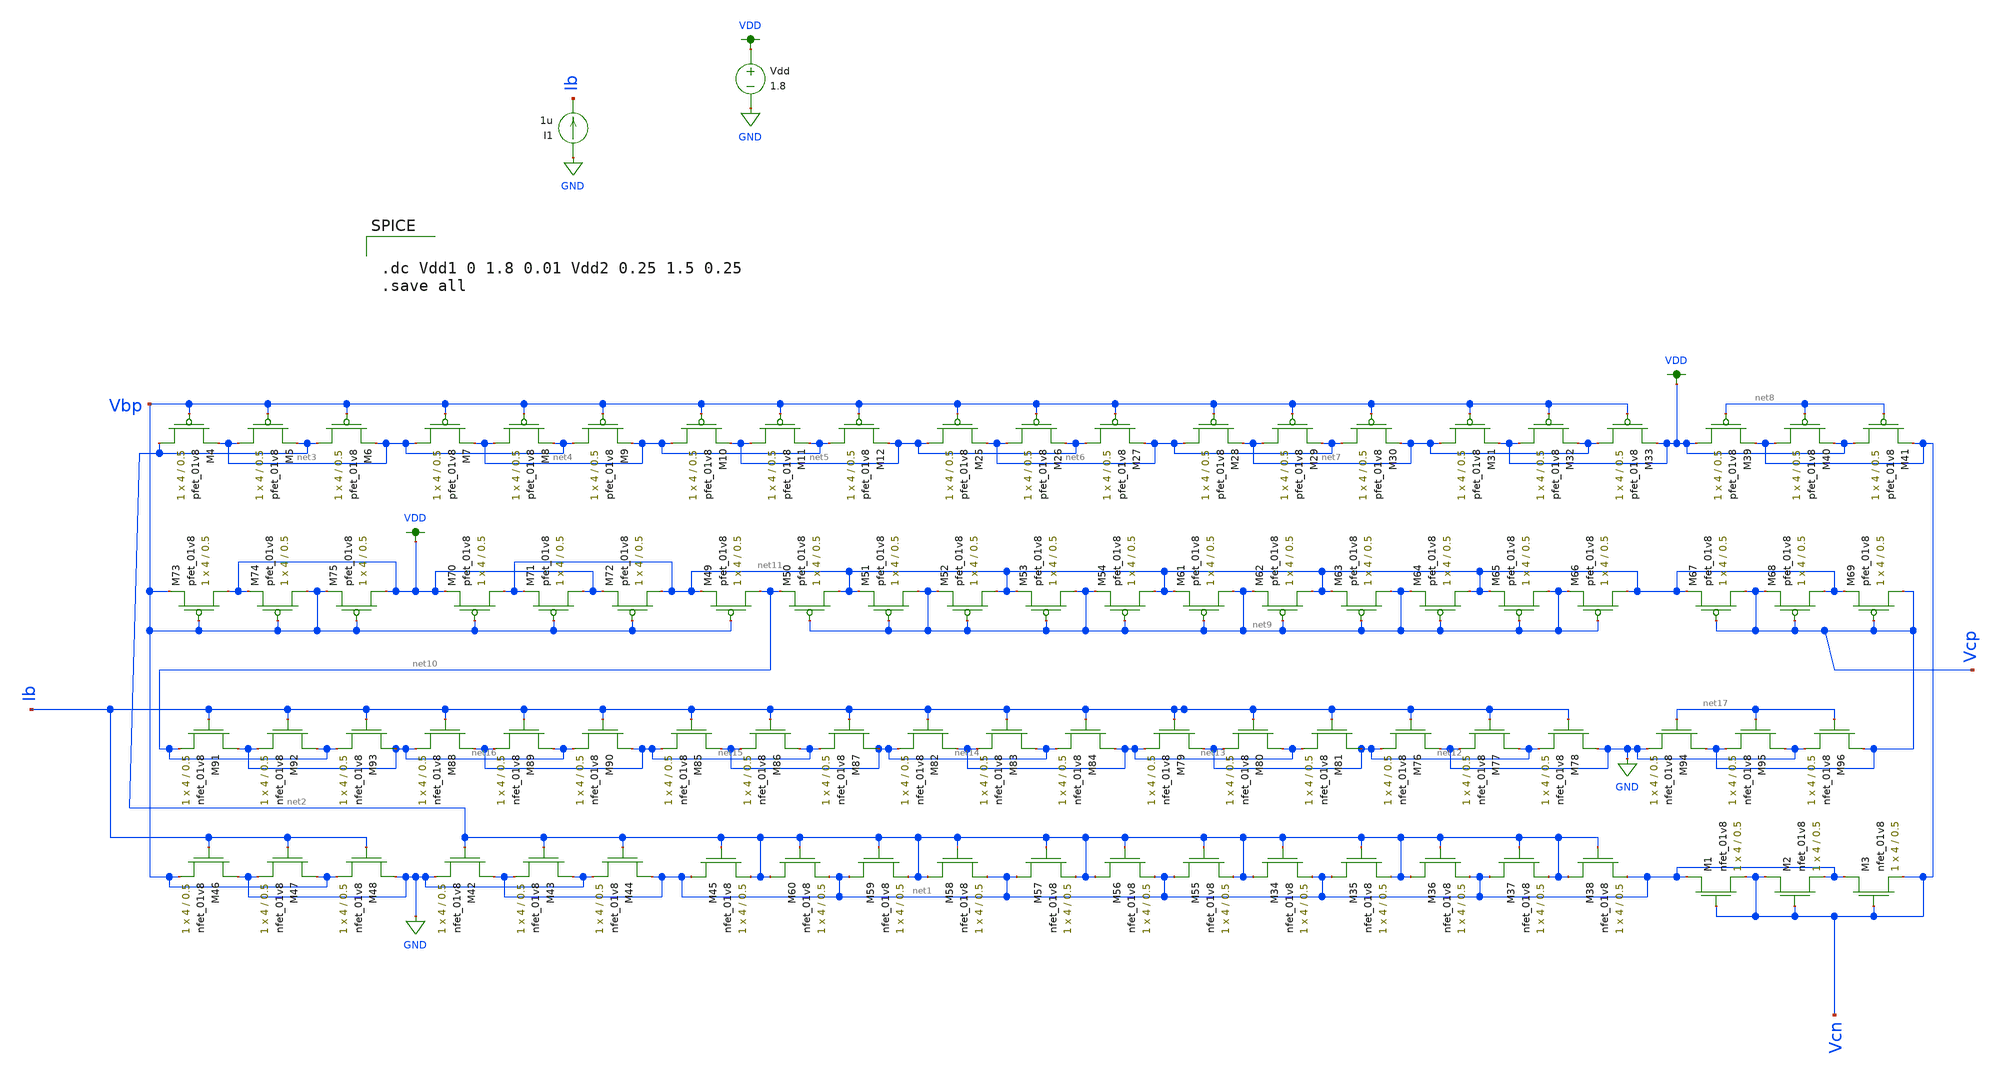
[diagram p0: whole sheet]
** sch_path: mp3/schematic/bias_lds.sch
**.subckt bias_lds
XM55 net1 net2 net2 GND sky130_fd_pr__nfet_01v8 L=0.5 W=4 nf=1 ad='int((nf+1)/2) * W/nf * 0.29' as='int((nf+2)/2) * W/nf * 0.29'
+ pd='2*int((nf+1)/2) * (W/nf + 0.29)' ps='2*int((nf+2)/2) * (W/nf + 0.29)' nrd='0.29 / W' nrs='0.29 / W'
+ sa=0 sb=0 sd=0 mult=1 m=1
XM56 net2 net2 net1 GND sky130_fd_pr__nfet_01v8 L=0.5 W=4 nf=1 ad='int((nf+1)/2) * W/nf * 0.29' as='int((nf+2)/2) * W/nf * 0.29'
+ pd='2*int((nf+1)/2) * (W/nf + 0.29)' ps='2*int((nf+2)/2) * (W/nf + 0.29)' nrd='0.29 / W' nrs='0.29 / W'
+ sa=0 sb=0 sd=0 mult=1 m=1
XM57 net1 net2 net2 GND sky130_fd_pr__nfet_01v8 L=0.5 W=4 nf=1 ad='int((nf+1)/2) * W/nf * 0.29' as='int((nf+2)/2) * W/nf * 0.29'
+ pd='2*int((nf+1)/2) * (W/nf + 0.29)' ps='2*int((nf+2)/2) * (W/nf + 0.29)' nrd='0.29 / W' nrs='0.29 / W'
+ sa=0 sb=0 sd=0 mult=1 m=1
XM58 net2 net2 net1 GND sky130_fd_pr__nfet_01v8 L=0.5 W=4 nf=1 ad='int((nf+1)/2) * W/nf * 0.29' as='int((nf+2)/2) * W/nf * 0.29'
+ pd='2*int((nf+1)/2) * (W/nf + 0.29)' ps='2*int((nf+2)/2) * (W/nf + 0.29)' nrd='0.29 / W' nrs='0.29 / W'
+ sa=0 sb=0 sd=0 mult=1 m=1
XM59 net1 net2 net2 GND sky130_fd_pr__nfet_01v8 L=0.5 W=4 nf=1 ad='int((nf+1)/2) * W/nf * 0.29' as='int((nf+2)/2) * W/nf * 0.29'
+ pd='2*int((nf+1)/2) * (W/nf + 0.29)' ps='2*int((nf+2)/2) * (W/nf + 0.29)' nrd='0.29 / W' nrs='0.29 / W'
+ sa=0 sb=0 sd=0 mult=1 m=1
XM60 net2 net2 net1 GND sky130_fd_pr__nfet_01v8 L=0.5 W=4 nf=1 ad='int((nf+1)/2) * W/nf * 0.29' as='int((nf+2)/2) * W/nf * 0.29'
+ pd='2*int((nf+1)/2) * (W/nf + 0.29)' ps='2*int((nf+2)/2) * (W/nf + 0.29)' nrd='0.29 / W' nrs='0.29 / W'
+ sa=0 sb=0 sd=0 mult=1 m=1
XM34 net2 net2 net1 GND sky130_fd_pr__nfet_01v8 L=0.5 W=4 nf=1 ad='int((nf+1)/2) * W/nf * 0.29' as='int((nf+2)/2) * W/nf * 0.29'
+ pd='2*int((nf+1)/2) * (W/nf + 0.29)' ps='2*int((nf+2)/2) * (W/nf + 0.29)' nrd='0.29 / W' nrs='0.29 / W'
+ sa=0 sb=0 sd=0 mult=1 m=1
XM35 net1 net2 net2 GND sky130_fd_pr__nfet_01v8 L=0.5 W=4 nf=1 ad='int((nf+1)/2) * W/nf * 0.29' as='int((nf+2)/2) * W/nf * 0.29'
+ pd='2*int((nf+1)/2) * (W/nf + 0.29)' ps='2*int((nf+2)/2) * (W/nf + 0.29)' nrd='0.29 / W' nrs='0.29 / W'
+ sa=0 sb=0 sd=0 mult=1 m=1
XM36 net2 net2 net1 GND sky130_fd_pr__nfet_01v8 L=0.5 W=4 nf=1 ad='int((nf+1)/2) * W/nf * 0.29' as='int((nf+2)/2) * W/nf * 0.29'
+ pd='2*int((nf+1)/2) * (W/nf + 0.29)' ps='2*int((nf+2)/2) * (W/nf + 0.29)' nrd='0.29 / W' nrs='0.29 / W'
+ sa=0 sb=0 sd=0 mult=1 m=1
XM37 net1 net2 net2 GND sky130_fd_pr__nfet_01v8 L=0.5 W=4 nf=1 ad='int((nf+1)/2) * W/nf * 0.29' as='int((nf+2)/2) * W/nf * 0.29'
+ pd='2*int((nf+1)/2) * (W/nf + 0.29)' ps='2*int((nf+2)/2) * (W/nf + 0.29)' nrd='0.29 / W' nrs='0.29 / W'
+ sa=0 sb=0 sd=0 mult=1 m=1
XM38 net2 net2 net1 GND sky130_fd_pr__nfet_01v8 L=0.5 W=4 nf=1 ad='int((nf+1)/2) * W/nf * 0.29' as='int((nf+2)/2) * W/nf * 0.29'
+ pd='2*int((nf+1)/2) * (W/nf + 0.29)' ps='2*int((nf+2)/2) * (W/nf + 0.29)' nrd='0.29 / W' nrs='0.29 / W'
+ sa=0 sb=0 sd=0 mult=1 m=1
XM45 net1 net2 net2 GND sky130_fd_pr__nfet_01v8 L=0.5 W=4 nf=1 ad='int((nf+1)/2) * W/nf * 0.29' as='int((nf+2)/2) * W/nf * 0.29'
+ pd='2*int((nf+1)/2) * (W/nf + 0.29)' ps='2*int((nf+2)/2) * (W/nf + 0.29)' nrd='0.29 / W' nrs='0.29 / W'
+ sa=0 sb=0 sd=0 mult=1 m=1
XM1 net1 Vcn Vcn GND sky130_fd_pr__nfet_01v8 L=0.5 W=4 nf=1 ad='int((nf+1)/2) * W/nf * 0.29' as='int((nf+2)/2) * W/nf * 0.29'
+ pd='2*int((nf+1)/2) * (W/nf + 0.29)' ps='2*int((nf+2)/2) * (W/nf + 0.29)' nrd='0.29 / W' nrs='0.29 / W'
+ sa=0 sb=0 sd=0 mult=1 m=1
XM2 Vcn Vcn net1 GND sky130_fd_pr__nfet_01v8 L=0.5 W=4 nf=1 ad='int((nf+1)/2) * W/nf * 0.29' as='int((nf+2)/2) * W/nf * 0.29'
+ pd='2*int((nf+1)/2) * (W/nf + 0.29)' ps='2*int((nf+2)/2) * (W/nf + 0.29)' nrd='0.29 / W' nrs='0.29 / W'
+ sa=0 sb=0 sd=0 mult=1 m=1
XM3 net1 Vcn Vcn GND sky130_fd_pr__nfet_01v8 L=0.5 W=4 nf=1 ad='int((nf+1)/2) * W/nf * 0.29' as='int((nf+2)/2) * W/nf * 0.29'
+ pd='2*int((nf+1)/2) * (W/nf + 0.29)' ps='2*int((nf+2)/2) * (W/nf + 0.29)' nrd='0.29 / W' nrs='0.29 / W'
+ sa=0 sb=0 sd=0 mult=1 m=1
XM4 net2 Vbp net3 VDD sky130_fd_pr__pfet_01v8 L=0.5 W=4 nf=1 ad='int((nf+1)/2) * W/nf * 0.29' as='int((nf+2)/2) * W/nf * 0.29'
+ pd='2*int((nf+1)/2) * (W/nf + 0.29)' ps='2*int((nf+2)/2) * (W/nf + 0.29)' nrd='0.29 / W' nrs='0.29 / W'
+ sa=0 sb=0 sd=0 mult=1 m=1
XM5 net3 Vbp net2 VDD sky130_fd_pr__pfet_01v8 L=0.5 W=4 nf=1 ad='int((nf+1)/2) * W/nf * 0.29' as='int((nf+2)/2) * W/nf * 0.29'
+ pd='2*int((nf+1)/2) * (W/nf + 0.29)' ps='2*int((nf+2)/2) * (W/nf + 0.29)' nrd='0.29 / W' nrs='0.29 / W'
+ sa=0 sb=0 sd=0 mult=1 m=1
XM6 net2 Vbp net3 VDD sky130_fd_pr__pfet_01v8 L=0.5 W=4 nf=1 ad='int((nf+1)/2) * W/nf * 0.29' as='int((nf+2)/2) * W/nf * 0.29'
+ pd='2*int((nf+1)/2) * (W/nf + 0.29)' ps='2*int((nf+2)/2) * (W/nf + 0.29)' nrd='0.29 / W' nrs='0.29 / W'
+ sa=0 sb=0 sd=0 mult=1 m=1
XM7 net3 Vbp net4 VDD sky130_fd_pr__pfet_01v8 L=0.5 W=4 nf=1 ad='int((nf+1)/2) * W/nf * 0.29' as='int((nf+2)/2) * W/nf * 0.29'
+ pd='2*int((nf+1)/2) * (W/nf + 0.29)' ps='2*int((nf+2)/2) * (W/nf + 0.29)' nrd='0.29 / W' nrs='0.29 / W'
+ sa=0 sb=0 sd=0 mult=1 m=1
XM8 net4 Vbp net3 VDD sky130_fd_pr__pfet_01v8 L=0.5 W=4 nf=1 ad='int((nf+1)/2) * W/nf * 0.29' as='int((nf+2)/2) * W/nf * 0.29'
+ pd='2*int((nf+1)/2) * (W/nf + 0.29)' ps='2*int((nf+2)/2) * (W/nf + 0.29)' nrd='0.29 / W' nrs='0.29 / W'
+ sa=0 sb=0 sd=0 mult=1 m=1
XM9 net3 Vbp net4 VDD sky130_fd_pr__pfet_01v8 L=0.5 W=4 nf=1 ad='int((nf+1)/2) * W/nf * 0.29' as='int((nf+2)/2) * W/nf * 0.29'
+ pd='2*int((nf+1)/2) * (W/nf + 0.29)' ps='2*int((nf+2)/2) * (W/nf + 0.29)' nrd='0.29 / W' nrs='0.29 / W'
+ sa=0 sb=0 sd=0 mult=1 m=1
XM10 net4 Vbp net5 VDD sky130_fd_pr__pfet_01v8 L=0.5 W=4 nf=1 ad='int((nf+1)/2) * W/nf * 0.29' as='int((nf+2)/2) * W/nf * 0.29'
+ pd='2*int((nf+1)/2) * (W/nf + 0.29)' ps='2*int((nf+2)/2) * (W/nf + 0.29)' nrd='0.29 / W' nrs='0.29 / W'
+ sa=0 sb=0 sd=0 mult=1 m=1
XM11 net5 Vbp net4 VDD sky130_fd_pr__pfet_01v8 L=0.5 W=4 nf=1 ad='int((nf+1)/2) * W/nf * 0.29' as='int((nf+2)/2) * W/nf * 0.29'
+ pd='2*int((nf+1)/2) * (W/nf + 0.29)' ps='2*int((nf+2)/2) * (W/nf + 0.29)' nrd='0.29 / W' nrs='0.29 / W'
+ sa=0 sb=0 sd=0 mult=1 m=1
XM12 net4 Vbp net5 VDD sky130_fd_pr__pfet_01v8 L=0.5 W=4 nf=1 ad='int((nf+1)/2) * W/nf * 0.29' as='int((nf+2)/2) * W/nf * 0.29'
+ pd='2*int((nf+1)/2) * (W/nf + 0.29)' ps='2*int((nf+2)/2) * (W/nf + 0.29)' nrd='0.29 / W' nrs='0.29 / W'
+ sa=0 sb=0 sd=0 mult=1 m=1
XM25 net5 Vbp net6 VDD sky130_fd_pr__pfet_01v8 L=0.5 W=4 nf=1 ad='int((nf+1)/2) * W/nf * 0.29' as='int((nf+2)/2) * W/nf * 0.29'
+ pd='2*int((nf+1)/2) * (W/nf + 0.29)' ps='2*int((nf+2)/2) * (W/nf + 0.29)' nrd='0.29 / W' nrs='0.29 / W'
+ sa=0 sb=0 sd=0 mult=1 m=1
XM26 net6 Vbp net5 VDD sky130_fd_pr__pfet_01v8 L=0.5 W=4 nf=1 ad='int((nf+1)/2) * W/nf * 0.29' as='int((nf+2)/2) * W/nf * 0.29'
+ pd='2*int((nf+1)/2) * (W/nf + 0.29)' ps='2*int((nf+2)/2) * (W/nf + 0.29)' nrd='0.29 / W' nrs='0.29 / W'
+ sa=0 sb=0 sd=0 mult=1 m=1
XM27 net5 Vbp net6 VDD sky130_fd_pr__pfet_01v8 L=0.5 W=4 nf=1 ad='int((nf+1)/2) * W/nf * 0.29' as='int((nf+2)/2) * W/nf * 0.29'
+ pd='2*int((nf+1)/2) * (W/nf + 0.29)' ps='2*int((nf+2)/2) * (W/nf + 0.29)' nrd='0.29 / W' nrs='0.29 / W'
+ sa=0 sb=0 sd=0 mult=1 m=1
XM28 net6 Vbp net7 VDD sky130_fd_pr__pfet_01v8 L=0.5 W=4 nf=1 ad='int((nf+1)/2) * W/nf * 0.29' as='int((nf+2)/2) * W/nf * 0.29'
+ pd='2*int((nf+1)/2) * (W/nf + 0.29)' ps='2*int((nf+2)/2) * (W/nf + 0.29)' nrd='0.29 / W' nrs='0.29 / W'
+ sa=0 sb=0 sd=0 mult=1 m=1
XM29 net7 Vbp net6 VDD sky130_fd_pr__pfet_01v8 L=0.5 W=4 nf=1 ad='int((nf+1)/2) * W/nf * 0.29' as='int((nf+2)/2) * W/nf * 0.29'
+ pd='2*int((nf+1)/2) * (W/nf + 0.29)' ps='2*int((nf+2)/2) * (W/nf + 0.29)' nrd='0.29 / W' nrs='0.29 / W'
+ sa=0 sb=0 sd=0 mult=1 m=1
XM30 net6 Vbp net7 VDD sky130_fd_pr__pfet_01v8 L=0.5 W=4 nf=1 ad='int((nf+1)/2) * W/nf * 0.29' as='int((nf+2)/2) * W/nf * 0.29'
+ pd='2*int((nf+1)/2) * (W/nf + 0.29)' ps='2*int((nf+2)/2) * (W/nf + 0.29)' nrd='0.29 / W' nrs='0.29 / W'
+ sa=0 sb=0 sd=0 mult=1 m=1
XM31 net7 Vbp VDD VDD sky130_fd_pr__pfet_01v8 L=0.5 W=4 nf=1 ad='int((nf+1)/2) * W/nf * 0.29' as='int((nf+2)/2) * W/nf * 0.29'
+ pd='2*int((nf+1)/2) * (W/nf + 0.29)' ps='2*int((nf+2)/2) * (W/nf + 0.29)' nrd='0.29 / W' nrs='0.29 / W'
+ sa=0 sb=0 sd=0 mult=1 m=1
XM32 VDD Vbp net7 VDD sky130_fd_pr__pfet_01v8 L=0.5 W=4 nf=1 ad='int((nf+1)/2) * W/nf * 0.29' as='int((nf+2)/2) * W/nf * 0.29'
+ pd='2*int((nf+1)/2) * (W/nf + 0.29)' ps='2*int((nf+2)/2) * (W/nf + 0.29)' nrd='0.29 / W' nrs='0.29 / W'
+ sa=0 sb=0 sd=0 mult=1 m=1
XM33 net7 Vbp VDD VDD sky130_fd_pr__pfet_01v8 L=0.5 W=4 nf=1 ad='int((nf+1)/2) * W/nf * 0.29' as='int((nf+2)/2) * W/nf * 0.29'
+ pd='2*int((nf+1)/2) * (W/nf + 0.29)' ps='2*int((nf+2)/2) * (W/nf + 0.29)' nrd='0.29 / W' nrs='0.29 / W'
+ sa=0 sb=0 sd=0 mult=1 m=1
XM39 VDD net8 Vcn VDD sky130_fd_pr__pfet_01v8 L=0.5 W=4 nf=1 ad='int((nf+1)/2) * W/nf * 0.29' as='int((nf+2)/2) * W/nf * 0.29'
+ pd='2*int((nf+1)/2) * (W/nf + 0.29)' ps='2*int((nf+2)/2) * (W/nf + 0.29)' nrd='0.29 / W' nrs='0.29 / W'
+ sa=0 sb=0 sd=0 mult=1 m=1
XM40 Vcn net8 VDD VDD sky130_fd_pr__pfet_01v8 L=0.5 W=4 nf=1 ad='int((nf+1)/2) * W/nf * 0.29' as='int((nf+2)/2) * W/nf * 0.29'
+ pd='2*int((nf+1)/2) * (W/nf + 0.29)' ps='2*int((nf+2)/2) * (W/nf + 0.29)' nrd='0.29 / W' nrs='0.29 / W'
+ sa=0 sb=0 sd=0 mult=1 m=1
XM41 VDD net8 Vcn VDD sky130_fd_pr__pfet_01v8 L=0.5 W=4 nf=1 ad='int((nf+1)/2) * W/nf * 0.29' as='int((nf+2)/2) * W/nf * 0.29'
+ pd='2*int((nf+1)/2) * (W/nf + 0.29)' ps='2*int((nf+2)/2) * (W/nf + 0.29)' nrd='0.29 / W' nrs='0.29 / W'
+ sa=0 sb=0 sd=0 mult=1 m=1
XM42 net1 net2 GND GND sky130_fd_pr__nfet_01v8 L=0.5 W=4 nf=1 ad='int((nf+1)/2) * W/nf * 0.29' as='int((nf+2)/2) * W/nf * 0.29'
+ pd='2*int((nf+1)/2) * (W/nf + 0.29)' ps='2*int((nf+2)/2) * (W/nf + 0.29)' nrd='0.29 / W' nrs='0.29 / W'
+ sa=0 sb=0 sd=0 mult=1 m=1
XM43 GND net2 net1 GND sky130_fd_pr__nfet_01v8 L=0.5 W=4 nf=1 ad='int((nf+1)/2) * W/nf * 0.29' as='int((nf+2)/2) * W/nf * 0.29'
+ pd='2*int((nf+1)/2) * (W/nf + 0.29)' ps='2*int((nf+2)/2) * (W/nf + 0.29)' nrd='0.29 / W' nrs='0.29 / W'
+ sa=0 sb=0 sd=0 mult=1 m=1
XM44 net1 net2 GND GND sky130_fd_pr__nfet_01v8 L=0.5 W=4 nf=1 ad='int((nf+1)/2) * W/nf * 0.29' as='int((nf+2)/2) * W/nf * 0.29'
+ pd='2*int((nf+1)/2) * (W/nf + 0.29)' ps='2*int((nf+2)/2) * (W/nf + 0.29)' nrd='0.29 / W' nrs='0.29 / W'
+ sa=0 sb=0 sd=0 mult=1 m=1
XM46 GND Ib Vbp GND sky130_fd_pr__nfet_01v8 L=0.5 W=4 nf=1 ad='int((nf+1)/2) * W/nf * 0.29' as='int((nf+2)/2) * W/nf * 0.29'
+ pd='2*int((nf+1)/2) * (W/nf + 0.29)' ps='2*int((nf+2)/2) * (W/nf + 0.29)' nrd='0.29 / W' nrs='0.29 / W'
+ sa=0 sb=0 sd=0 mult=1 m=1
XM47 Vbp Ib GND GND sky130_fd_pr__nfet_01v8 L=0.5 W=4 nf=1 ad='int((nf+1)/2) * W/nf * 0.29' as='int((nf+2)/2) * W/nf * 0.29'
+ pd='2*int((nf+1)/2) * (W/nf + 0.29)' ps='2*int((nf+2)/2) * (W/nf + 0.29)' nrd='0.29 / W' nrs='0.29 / W'
+ sa=0 sb=0 sd=0 mult=1 m=1
XM48 GND Ib Vbp GND sky130_fd_pr__nfet_01v8 L=0.5 W=4 nf=1 ad='int((nf+1)/2) * W/nf * 0.29' as='int((nf+2)/2) * W/nf * 0.29'
+ pd='2*int((nf+1)/2) * (W/nf + 0.29)' ps='2*int((nf+2)/2) * (W/nf + 0.29)' nrd='0.29 / W' nrs='0.29 / W'
+ sa=0 sb=0 sd=0 mult=1 m=1
XM49 net10 Vbp net11 VDD sky130_fd_pr__pfet_01v8 L=0.5 W=4 nf=1 ad='int((nf+1)/2) * W/nf * 0.29' as='int((nf+2)/2) * W/nf * 0.29'
+ pd='2*int((nf+1)/2) * (W/nf + 0.29)' ps='2*int((nf+2)/2) * (W/nf + 0.29)' nrd='0.29 / W' nrs='0.29 / W'
+ sa=0 sb=0 sd=0 mult=1 m=1
XM50 net11 net9 net10 VDD sky130_fd_pr__pfet_01v8 L=0.5 W=4 nf=1 ad='int((nf+1)/2) * W/nf * 0.29' as='int((nf+2)/2) * W/nf * 0.29'
+ pd='2*int((nf+1)/2) * (W/nf + 0.29)' ps='2*int((nf+2)/2) * (W/nf + 0.29)' nrd='0.29 / W' nrs='0.29 / W'
+ sa=0 sb=0 sd=0 mult=1 m=1
XM51 net9 net9 net11 VDD sky130_fd_pr__pfet_01v8 L=0.5 W=4 nf=1 ad='int((nf+1)/2) * W/nf * 0.29' as='int((nf+2)/2) * W/nf * 0.29'
+ pd='2*int((nf+1)/2) * (W/nf + 0.29)' ps='2*int((nf+2)/2) * (W/nf + 0.29)' nrd='0.29 / W' nrs='0.29 / W'
+ sa=0 sb=0 sd=0 mult=1 m=1
XM52 net11 net9 net9 VDD sky130_fd_pr__pfet_01v8 L=0.5 W=4 nf=1 ad='int((nf+1)/2) * W/nf * 0.29' as='int((nf+2)/2) * W/nf * 0.29'
+ pd='2*int((nf+1)/2) * (W/nf + 0.29)' ps='2*int((nf+2)/2) * (W/nf + 0.29)' nrd='0.29 / W' nrs='0.29 / W'
+ sa=0 sb=0 sd=0 mult=1 m=1
XM53 net9 net9 net11 VDD sky130_fd_pr__pfet_01v8 L=0.5 W=4 nf=1 ad='int((nf+1)/2) * W/nf * 0.29' as='int((nf+2)/2) * W/nf * 0.29'
+ pd='2*int((nf+1)/2) * (W/nf + 0.29)' ps='2*int((nf+2)/2) * (W/nf + 0.29)' nrd='0.29 / W' nrs='0.29 / W'
+ sa=0 sb=0 sd=0 mult=1 m=1
XM54 net11 net9 net9 VDD sky130_fd_pr__pfet_01v8 L=0.5 W=4 nf=1 ad='int((nf+1)/2) * W/nf * 0.29' as='int((nf+2)/2) * W/nf * 0.29'
+ pd='2*int((nf+1)/2) * (W/nf + 0.29)' ps='2*int((nf+2)/2) * (W/nf + 0.29)' nrd='0.29 / W' nrs='0.29 / W'
+ sa=0 sb=0 sd=0 mult=1 m=1
XM61 net9 net9 net11 VDD sky130_fd_pr__pfet_01v8 L=0.5 W=4 nf=1 ad='int((nf+1)/2) * W/nf * 0.29' as='int((nf+2)/2) * W/nf * 0.29'
+ pd='2*int((nf+1)/2) * (W/nf + 0.29)' ps='2*int((nf+2)/2) * (W/nf + 0.29)' nrd='0.29 / W' nrs='0.29 / W'
+ sa=0 sb=0 sd=0 mult=1 m=1
XM62 net11 net9 net9 VDD sky130_fd_pr__pfet_01v8 L=0.5 W=4 nf=1 ad='int((nf+1)/2) * W/nf * 0.29' as='int((nf+2)/2) * W/nf * 0.29'
+ pd='2*int((nf+1)/2) * (W/nf + 0.29)' ps='2*int((nf+2)/2) * (W/nf + 0.29)' nrd='0.29 / W' nrs='0.29 / W'
+ sa=0 sb=0 sd=0 mult=1 m=1
XM63 net9 net9 net11 VDD sky130_fd_pr__pfet_01v8 L=0.5 W=4 nf=1 ad='int((nf+1)/2) * W/nf * 0.29' as='int((nf+2)/2) * W/nf * 0.29'
+ pd='2*int((nf+1)/2) * (W/nf + 0.29)' ps='2*int((nf+2)/2) * (W/nf + 0.29)' nrd='0.29 / W' nrs='0.29 / W'
+ sa=0 sb=0 sd=0 mult=1 m=1
XM64 net11 net9 net9 VDD sky130_fd_pr__pfet_01v8 L=0.5 W=4 nf=1 ad='int((nf+1)/2) * W/nf * 0.29' as='int((nf+2)/2) * W/nf * 0.29'
+ pd='2*int((nf+1)/2) * (W/nf + 0.29)' ps='2*int((nf+2)/2) * (W/nf + 0.29)' nrd='0.29 / W' nrs='0.29 / W'
+ sa=0 sb=0 sd=0 mult=1 m=1
XM65 net9 net9 net11 VDD sky130_fd_pr__pfet_01v8 L=0.5 W=4 nf=1 ad='int((nf+1)/2) * W/nf * 0.29' as='int((nf+2)/2) * W/nf * 0.29'
+ pd='2*int((nf+1)/2) * (W/nf + 0.29)' ps='2*int((nf+2)/2) * (W/nf + 0.29)' nrd='0.29 / W' nrs='0.29 / W'
+ sa=0 sb=0 sd=0 mult=1 m=1
XM66 net11 net9 net9 VDD sky130_fd_pr__pfet_01v8 L=0.5 W=4 nf=1 ad='int((nf+1)/2) * W/nf * 0.29' as='int((nf+2)/2) * W/nf * 0.29'
+ pd='2*int((nf+1)/2) * (W/nf + 0.29)' ps='2*int((nf+2)/2) * (W/nf + 0.29)' nrd='0.29 / W' nrs='0.29 / W'
+ sa=0 sb=0 sd=0 mult=1 m=1
XM67 Vcp Vcp net11 VDD sky130_fd_pr__pfet_01v8 L=0.5 W=4 nf=1 ad='int((nf+1)/2) * W/nf * 0.29' as='int((nf+2)/2) * W/nf * 0.29'
+ pd='2*int((nf+1)/2) * (W/nf + 0.29)' ps='2*int((nf+2)/2) * (W/nf + 0.29)' nrd='0.29 / W' nrs='0.29 / W'
+ sa=0 sb=0 sd=0 mult=1 m=1
XM68 net11 Vcp Vcp VDD sky130_fd_pr__pfet_01v8 L=0.5 W=4 nf=1 ad='int((nf+1)/2) * W/nf * 0.29' as='int((nf+2)/2) * W/nf * 0.29'
+ pd='2*int((nf+1)/2) * (W/nf + 0.29)' ps='2*int((nf+2)/2) * (W/nf + 0.29)' nrd='0.29 / W' nrs='0.29 / W'
+ sa=0 sb=0 sd=0 mult=1 m=1
XM69 Vcp Vcp net11 VDD sky130_fd_pr__pfet_01v8 L=0.5 W=4 nf=1 ad='int((nf+1)/2) * W/nf * 0.29' as='int((nf+2)/2) * W/nf * 0.29'
+ pd='2*int((nf+1)/2) * (W/nf + 0.29)' ps='2*int((nf+2)/2) * (W/nf + 0.29)' nrd='0.29 / W' nrs='0.29 / W'
+ sa=0 sb=0 sd=0 mult=1 m=1
XM70 net11 Vbp VDD VDD sky130_fd_pr__pfet_01v8 L=0.5 W=4 nf=1 ad='int((nf+1)/2) * W/nf * 0.29' as='int((nf+2)/2) * W/nf * 0.29'
+ pd='2*int((nf+1)/2) * (W/nf + 0.29)' ps='2*int((nf+2)/2) * (W/nf + 0.29)' nrd='0.29 / W' nrs='0.29 / W'
+ sa=0 sb=0 sd=0 mult=1 m=1
XM71 VDD Vbp net11 VDD sky130_fd_pr__pfet_01v8 L=0.5 W=4 nf=1 ad='int((nf+1)/2) * W/nf * 0.29' as='int((nf+2)/2) * W/nf * 0.29'
+ pd='2*int((nf+1)/2) * (W/nf + 0.29)' ps='2*int((nf+2)/2) * (W/nf + 0.29)' nrd='0.29 / W' nrs='0.29 / W'
+ sa=0 sb=0 sd=0 mult=1 m=1
XM72 net11 Vbp VDD VDD sky130_fd_pr__pfet_01v8 L=0.5 W=4 nf=1 ad='int((nf+1)/2) * W/nf * 0.29' as='int((nf+2)/2) * W/nf * 0.29'
+ pd='2*int((nf+1)/2) * (W/nf + 0.29)' ps='2*int((nf+2)/2) * (W/nf + 0.29)' nrd='0.29 / W' nrs='0.29 / W'
+ sa=0 sb=0 sd=0 mult=1 m=1
XM73 VDD Vbp Vbp VDD sky130_fd_pr__pfet_01v8 L=0.5 W=4 nf=1 ad='int((nf+1)/2) * W/nf * 0.29' as='int((nf+2)/2) * W/nf * 0.29'
+ pd='2*int((nf+1)/2) * (W/nf + 0.29)' ps='2*int((nf+2)/2) * (W/nf + 0.29)' nrd='0.29 / W' nrs='0.29 / W'
+ sa=0 sb=0 sd=0 mult=1 m=1
XM74 Vbp Vbp VDD VDD sky130_fd_pr__pfet_01v8 L=0.5 W=4 nf=1 ad='int((nf+1)/2) * W/nf * 0.29' as='int((nf+2)/2) * W/nf * 0.29'
+ pd='2*int((nf+1)/2) * (W/nf + 0.29)' ps='2*int((nf+2)/2) * (W/nf + 0.29)' nrd='0.29 / W' nrs='0.29 / W'
+ sa=0 sb=0 sd=0 mult=1 m=1
XM75 VDD Vbp Vbp VDD sky130_fd_pr__pfet_01v8 L=0.5 W=4 nf=1 ad='int((nf+1)/2) * W/nf * 0.29' as='int((nf+2)/2) * W/nf * 0.29'
+ pd='2*int((nf+1)/2) * (W/nf + 0.29)' ps='2*int((nf+2)/2) * (W/nf + 0.29)' nrd='0.29 / W' nrs='0.29 / W'
+ sa=0 sb=0 sd=0 mult=1 m=1
XM76 GND Ib net12 GND sky130_fd_pr__nfet_01v8 L=0.5 W=4 nf=1 ad='int((nf+1)/2) * W/nf * 0.29' as='int((nf+2)/2) * W/nf * 0.29'
+ pd='2*int((nf+1)/2) * (W/nf + 0.29)' ps='2*int((nf+2)/2) * (W/nf + 0.29)' nrd='0.29 / W' nrs='0.29 / W'
+ sa=0 sb=0 sd=0 mult=1 m=1
XM77 net12 Ib GND GND sky130_fd_pr__nfet_01v8 L=0.5 W=4 nf=1 ad='int((nf+1)/2) * W/nf * 0.29' as='int((nf+2)/2) * W/nf * 0.29'
+ pd='2*int((nf+1)/2) * (W/nf + 0.29)' ps='2*int((nf+2)/2) * (W/nf + 0.29)' nrd='0.29 / W' nrs='0.29 / W'
+ sa=0 sb=0 sd=0 mult=1 m=1
XM78 GND Ib net12 GND sky130_fd_pr__nfet_01v8 L=0.5 W=4 nf=1 ad='int((nf+1)/2) * W/nf * 0.29' as='int((nf+2)/2) * W/nf * 0.29'
+ pd='2*int((nf+1)/2) * (W/nf + 0.29)' ps='2*int((nf+2)/2) * (W/nf + 0.29)' nrd='0.29 / W' nrs='0.29 / W'
+ sa=0 sb=0 sd=0 mult=1 m=1
XM79 net12 Ib net13 GND sky130_fd_pr__nfet_01v8 L=0.5 W=4 nf=1 ad='int((nf+1)/2) * W/nf * 0.29' as='int((nf+2)/2) * W/nf * 0.29'
+ pd='2*int((nf+1)/2) * (W/nf + 0.29)' ps='2*int((nf+2)/2) * (W/nf + 0.29)' nrd='0.29 / W' nrs='0.29 / W'
+ sa=0 sb=0 sd=0 mult=1 m=1
XM80 net13 Ib net12 GND sky130_fd_pr__nfet_01v8 L=0.5 W=4 nf=1 ad='int((nf+1)/2) * W/nf * 0.29' as='int((nf+2)/2) * W/nf * 0.29'
+ pd='2*int((nf+1)/2) * (W/nf + 0.29)' ps='2*int((nf+2)/2) * (W/nf + 0.29)' nrd='0.29 / W' nrs='0.29 / W'
+ sa=0 sb=0 sd=0 mult=1 m=1
XM81 net12 Ib net13 GND sky130_fd_pr__nfet_01v8 L=0.5 W=4 nf=1 ad='int((nf+1)/2) * W/nf * 0.29' as='int((nf+2)/2) * W/nf * 0.29'
+ pd='2*int((nf+1)/2) * (W/nf + 0.29)' ps='2*int((nf+2)/2) * (W/nf + 0.29)' nrd='0.29 / W' nrs='0.29 / W'
+ sa=0 sb=0 sd=0 mult=1 m=1
XM82 net13 Ib net14 GND sky130_fd_pr__nfet_01v8 L=0.5 W=4 nf=1 ad='int((nf+1)/2) * W/nf * 0.29' as='int((nf+2)/2) * W/nf * 0.29'
+ pd='2*int((nf+1)/2) * (W/nf + 0.29)' ps='2*int((nf+2)/2) * (W/nf + 0.29)' nrd='0.29 / W' nrs='0.29 / W'
+ sa=0 sb=0 sd=0 mult=1 m=1
XM83 net14 Ib net13 GND sky130_fd_pr__nfet_01v8 L=0.5 W=4 nf=1 ad='int((nf+1)/2) * W/nf * 0.29' as='int((nf+2)/2) * W/nf * 0.29'
+ pd='2*int((nf+1)/2) * (W/nf + 0.29)' ps='2*int((nf+2)/2) * (W/nf + 0.29)' nrd='0.29 / W' nrs='0.29 / W'
+ sa=0 sb=0 sd=0 mult=1 m=1
XM84 net13 Ib net14 GND sky130_fd_pr__nfet_01v8 L=0.5 W=4 nf=1 ad='int((nf+1)/2) * W/nf * 0.29' as='int((nf+2)/2) * W/nf * 0.29'
+ pd='2*int((nf+1)/2) * (W/nf + 0.29)' ps='2*int((nf+2)/2) * (W/nf + 0.29)' nrd='0.29 / W' nrs='0.29 / W'
+ sa=0 sb=0 sd=0 mult=1 m=1
XM85 net14 Ib net15 GND sky130_fd_pr__nfet_01v8 L=0.5 W=4 nf=1 ad='int((nf+1)/2) * W/nf * 0.29' as='int((nf+2)/2) * W/nf * 0.29'
+ pd='2*int((nf+1)/2) * (W/nf + 0.29)' ps='2*int((nf+2)/2) * (W/nf + 0.29)' nrd='0.29 / W' nrs='0.29 / W'
+ sa=0 sb=0 sd=0 mult=1 m=1
XM86 net15 Ib net14 GND sky130_fd_pr__nfet_01v8 L=0.5 W=4 nf=1 ad='int((nf+1)/2) * W/nf * 0.29' as='int((nf+2)/2) * W/nf * 0.29'
+ pd='2*int((nf+1)/2) * (W/nf + 0.29)' ps='2*int((nf+2)/2) * (W/nf + 0.29)' nrd='0.29 / W' nrs='0.29 / W'
+ sa=0 sb=0 sd=0 mult=1 m=1
XM87 net14 Ib net15 GND sky130_fd_pr__nfet_01v8 L=0.5 W=4 nf=1 ad='int((nf+1)/2) * W/nf * 0.29' as='int((nf+2)/2) * W/nf * 0.29'
+ pd='2*int((nf+1)/2) * (W/nf + 0.29)' ps='2*int((nf+2)/2) * (W/nf + 0.29)' nrd='0.29 / W' nrs='0.29 / W'
+ sa=0 sb=0 sd=0 mult=1 m=1
XM88 net15 Ib net16 GND sky130_fd_pr__nfet_01v8 L=0.5 W=4 nf=1 ad='int((nf+1)/2) * W/nf * 0.29' as='int((nf+2)/2) * W/nf * 0.29'
+ pd='2*int((nf+1)/2) * (W/nf + 0.29)' ps='2*int((nf+2)/2) * (W/nf + 0.29)' nrd='0.29 / W' nrs='0.29 / W'
+ sa=0 sb=0 sd=0 mult=1 m=1
XM89 net16 Ib net15 GND sky130_fd_pr__nfet_01v8 L=0.5 W=4 nf=1 ad='int((nf+1)/2) * W/nf * 0.29' as='int((nf+2)/2) * W/nf * 0.29'
+ pd='2*int((nf+1)/2) * (W/nf + 0.29)' ps='2*int((nf+2)/2) * (W/nf + 0.29)' nrd='0.29 / W' nrs='0.29 / W'
+ sa=0 sb=0 sd=0 mult=1 m=1
XM90 net15 Ib net16 GND sky130_fd_pr__nfet_01v8 L=0.5 W=4 nf=1 ad='int((nf+1)/2) * W/nf * 0.29' as='int((nf+2)/2) * W/nf * 0.29'
+ pd='2*int((nf+1)/2) * (W/nf + 0.29)' ps='2*int((nf+2)/2) * (W/nf + 0.29)' nrd='0.29 / W' nrs='0.29 / W'
+ sa=0 sb=0 sd=0 mult=1 m=1
XM91 net16 Ib net10 GND sky130_fd_pr__nfet_01v8 L=0.5 W=4 nf=1 ad='int((nf+1)/2) * W/nf * 0.29' as='int((nf+2)/2) * W/nf * 0.29'
+ pd='2*int((nf+1)/2) * (W/nf + 0.29)' ps='2*int((nf+2)/2) * (W/nf + 0.29)' nrd='0.29 / W' nrs='0.29 / W'
+ sa=0 sb=0 sd=0 mult=1 m=1
XM92 net10 Ib net16 GND sky130_fd_pr__nfet_01v8 L=0.5 W=4 nf=1 ad='int((nf+1)/2) * W/nf * 0.29' as='int((nf+2)/2) * W/nf * 0.29'
+ pd='2*int((nf+1)/2) * (W/nf + 0.29)' ps='2*int((nf+2)/2) * (W/nf + 0.29)' nrd='0.29 / W' nrs='0.29 / W'
+ sa=0 sb=0 sd=0 mult=1 m=1
XM93 net16 Ib net10 GND sky130_fd_pr__nfet_01v8 L=0.5 W=4 nf=1 ad='int((nf+1)/2) * W/nf * 0.29' as='int((nf+2)/2) * W/nf * 0.29'
+ pd='2*int((nf+1)/2) * (W/nf + 0.29)' ps='2*int((nf+2)/2) * (W/nf + 0.29)' nrd='0.29 / W' nrs='0.29 / W'
+ sa=0 sb=0 sd=0 mult=1 m=1
XM94 Vcp net17 GND GND sky130_fd_pr__nfet_01v8 L=0.5 W=4 nf=1 ad='int((nf+1)/2) * W/nf * 0.29' as='int((nf+2)/2) * W/nf * 0.29'
+ pd='2*int((nf+1)/2) * (W/nf + 0.29)' ps='2*int((nf+2)/2) * (W/nf + 0.29)' nrd='0.29 / W' nrs='0.29 / W'
+ sa=0 sb=0 sd=0 mult=1 m=1
XM95 GND net17 Vcp GND sky130_fd_pr__nfet_01v8 L=0.5 W=4 nf=1 ad='int((nf+1)/2) * W/nf * 0.29' as='int((nf+2)/2) * W/nf * 0.29'
+ pd='2*int((nf+1)/2) * (W/nf + 0.29)' ps='2*int((nf+2)/2) * (W/nf + 0.29)' nrd='0.29 / W' nrs='0.29 / W'
+ sa=0 sb=0 sd=0 mult=1 m=1
XM96 Vcp net17 GND GND sky130_fd_pr__nfet_01v8 L=0.5 W=4 nf=1 ad='int((nf+1)/2) * W/nf * 0.29' as='int((nf+2)/2) * W/nf * 0.29'
+ pd='2*int((nf+1)/2) * (W/nf + 0.29)' ps='2*int((nf+2)/2) * (W/nf + 0.29)' nrd='0.29 / W' nrs='0.29 / W'
+ sa=0 sb=0 sd=0 mult=1 m=1
I1 GND Ib 1u
Vdd VDD GND 1.8
**** begin user architecture code

.option wnflag=1
.lib ~/skywater/skywater-pdk/libraries/sky130_fd_pr_ngspice/latest/models/sky130.lib.spice tt



.dc Vdd1 0 1.8 0.01 Vdd2 0.25 1.5 0.25
.save all

**** end user architecture code
**.ends
.GLOBAL VDD
.GLOBAL GND
.end
